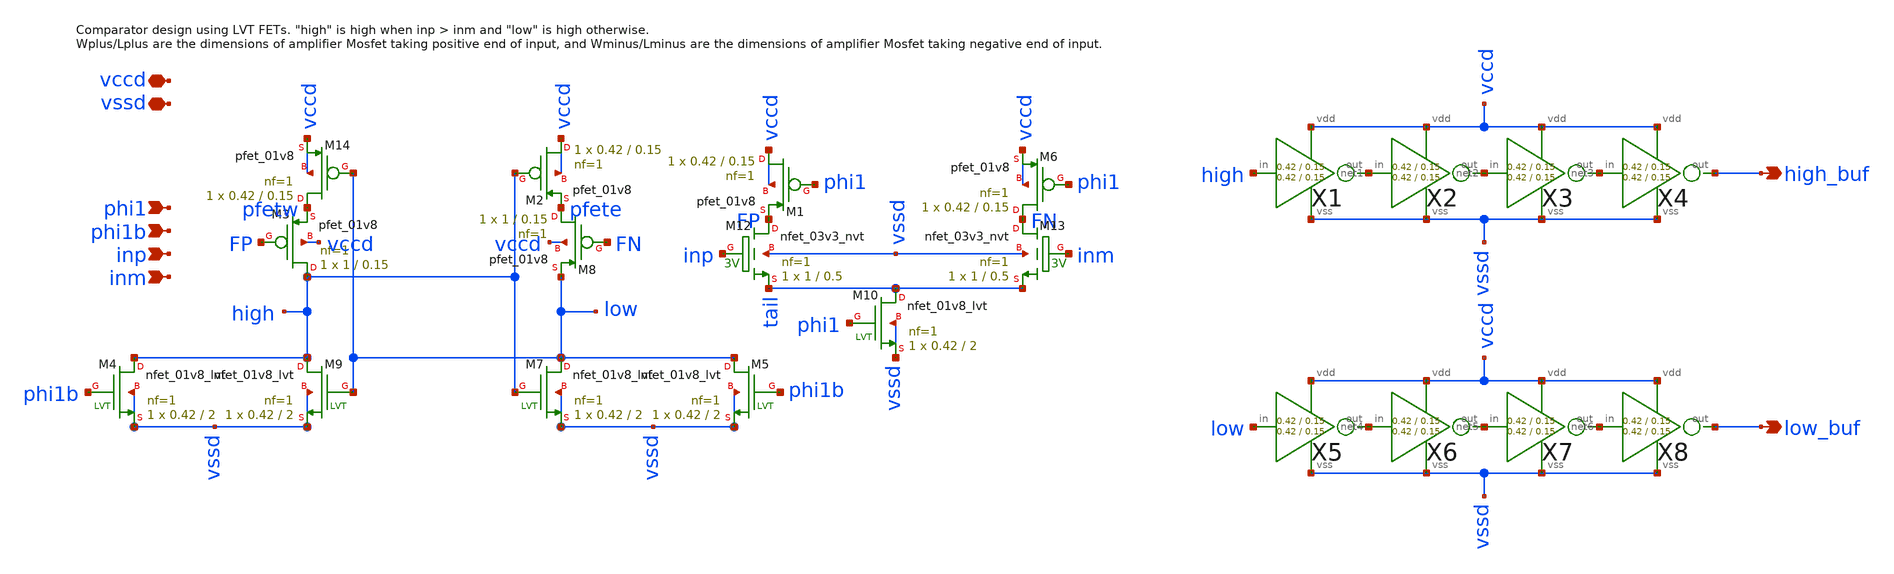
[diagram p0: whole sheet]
** sch_path: xschem/comparator_latest/comparator_single_tail.sch
**.subckt comparator_single_tail phi1 phi1b inp inm low_buf vccd vssd high_buf
*.ipin phi1
*.ipin phi1b
*.ipin inp
*.ipin inm
*.opin low_buf
*.iopin vccd
*.iopin vssd
*.opin high_buf
XM12 FP inp tail vssd sky130_fd_pr__nfet_03v3_nvt L=0.5 W=1 nf=1 ad='int((nf+1)/2) * W/nf * 0.29' as='int((nf+2)/2) * W/nf * 0.29'
+ pd='2*int((nf+1)/2) * (W/nf + 0.29)' ps='2*int((nf+2)/2) * (W/nf + 0.29)' nrd='0.29 / W' nrs='0.29 / W'
+ sa=0 sb=0 sd=0 mult=1 m=1
XM13 FN inm tail vssd sky130_fd_pr__nfet_03v3_nvt L=0.5 W=1 nf=1 ad='int((nf+1)/2) * W/nf * 0.29' as='int((nf+2)/2) * W/nf * 0.29'
+ pd='2*int((nf+1)/2) * (W/nf + 0.29)' ps='2*int((nf+2)/2) * (W/nf + 0.29)' nrd='0.29 / W' nrs='0.29 / W'
+ sa=0 sb=0 sd=0 mult=1 m=1
XM14 pfetw low vccd vccd sky130_fd_pr__pfet_01v8 L=0.15 W=0.42 nf=1 ad='int((nf+1)/2) * W/nf * 0.29'
+ as='int((nf+2)/2) * W/nf * 0.29' pd='2*int((nf+1)/2) * (W/nf + 0.29)' ps='2*int((nf+2)/2) * (W/nf + 0.29)'
+ nrd='0.29 / W' nrs='0.29 / W' sa=0 sb=0 sd=0 mult=1 m=1
XM3 high FP pfetw vccd sky130_fd_pr__pfet_01v8 L=0.15 W=1 nf=1 ad='int((nf+1)/2) * W/nf * 0.29' as='int((nf+2)/2) * W/nf * 0.29'
+ pd='2*int((nf+1)/2) * (W/nf + 0.29)' ps='2*int((nf+2)/2) * (W/nf + 0.29)' nrd='0.29 / W' nrs='0.29 / W'
+ sa=0 sb=0 sd=0 mult=1 m=1
XM8 pfete FN low vccd sky130_fd_pr__pfet_01v8 L=0.15 W=1 nf=1 ad='int((nf+1)/2) * W/nf * 0.29' as='int((nf+2)/2) * W/nf * 0.29'
+ pd='2*int((nf+1)/2) * (W/nf + 0.29)' ps='2*int((nf+2)/2) * (W/nf + 0.29)' nrd='0.29 / W' nrs='0.29 / W'
+ sa=0 sb=0 sd=0 mult=1 m=1
XM2 vccd high pfete vccd sky130_fd_pr__pfet_01v8 L=0.15 W=0.42 nf=1 ad='int((nf+1)/2) * W/nf * 0.29'
+ as='int((nf+2)/2) * W/nf * 0.29' pd='2*int((nf+1)/2) * (W/nf + 0.29)' ps='2*int((nf+2)/2) * (W/nf + 0.29)'
+ nrd='0.29 / W' nrs='0.29 / W' sa=0 sb=0 sd=0 mult=1 m=1
XM7 low high vssd vssd sky130_fd_pr__nfet_01v8_lvt L=2 W=0.42 nf=1 ad='int((nf+1)/2) * W/nf * 0.29' as='int((nf+2)/2) * W/nf * 0.29'
+ pd='2*int((nf+1)/2) * (W/nf + 0.29)' ps='2*int((nf+2)/2) * (W/nf + 0.29)' nrd='0.29 / W' nrs='0.29 / W'
+ sa=0 sb=0 sd=0 mult=1 m=1
XM9 high low vssd vssd sky130_fd_pr__nfet_01v8_lvt L=2 W=0.42 nf=1 ad='int((nf+1)/2) * W/nf * 0.29' as='int((nf+2)/2) * W/nf * 0.29'
+ pd='2*int((nf+1)/2) * (W/nf + 0.29)' ps='2*int((nf+2)/2) * (W/nf + 0.29)' nrd='0.29 / W' nrs='0.29 / W'
+ sa=0 sb=0 sd=0 mult=1 m=1
XM10 tail phi1 vssd vssd sky130_fd_pr__nfet_01v8_lvt L=2 W=0.42 nf=1 ad='int((nf+1)/2) * W/nf * 0.29'
+ as='int((nf+2)/2) * W/nf * 0.29' pd='2*int((nf+1)/2) * (W/nf + 0.29)' ps='2*int((nf+2)/2) * (W/nf + 0.29)'
+ nrd='0.29 / W' nrs='0.29 / W' sa=0 sb=0 sd=0 mult=1 m=1
XM1 vccd phi1 FP vccd sky130_fd_pr__pfet_01v8 L=0.15 W=0.42 nf=1 ad='int((nf+1)/2) * W/nf * 0.29' as='int((nf+2)/2) * W/nf * 0.29'
+ pd='2*int((nf+1)/2) * (W/nf + 0.29)' ps='2*int((nf+2)/2) * (W/nf + 0.29)' nrd='0.29 / W' nrs='0.29 / W'
+ sa=0 sb=0 sd=0 mult=1 m=1
XM6 FN phi1 vccd vccd sky130_fd_pr__pfet_01v8 L=0.15 W=0.42 nf=1 ad='int((nf+1)/2) * W/nf * 0.29' as='int((nf+2)/2) * W/nf * 0.29'
+ pd='2*int((nf+1)/2) * (W/nf + 0.29)' ps='2*int((nf+2)/2) * (W/nf + 0.29)' nrd='0.29 / W' nrs='0.29 / W'
+ sa=0 sb=0 sd=0 mult=1 m=1
X1 high net1 vccd vssd inv Wpmos=0.42 Lpmos=0.15 Wnmos=0.42 Lnmos=0.15
X2 net1 net2 vccd vssd inv Wpmos=0.42 Lpmos=0.15 Wnmos=0.42 Lnmos=0.15
X3 net2 net3 vccd vssd inv Wpmos=0.42 Lpmos=0.15 Wnmos=0.42 Lnmos=0.15
X4 net3 high_buf vccd vssd inv Wpmos=0.42 Lpmos=0.15 Wnmos=0.42 Lnmos=0.15
X5 low net4 vccd vssd inv Wpmos=0.42 Lpmos=0.15 Wnmos=0.42 Lnmos=0.15
X6 net4 net5 vccd vssd inv Wpmos=0.42 Lpmos=0.15 Wnmos=0.42 Lnmos=0.15
X7 net5 net6 vccd vssd inv Wpmos=0.42 Lpmos=0.15 Wnmos=0.42 Lnmos=0.15
X8 net6 low_buf vccd vssd inv Wpmos=0.42 Lpmos=0.15 Wnmos=0.42 Lnmos=0.15
XM4 high phi1b vssd vssd sky130_fd_pr__nfet_01v8_lvt L=2 W=0.42 nf=1 ad='int((nf+1)/2) * W/nf * 0.29'
+ as='int((nf+2)/2) * W/nf * 0.29' pd='2*int((nf+1)/2) * (W/nf + 0.29)' ps='2*int((nf+2)/2) * (W/nf + 0.29)'
+ nrd='0.29 / W' nrs='0.29 / W' sa=0 sb=0 sd=0 mult=1 m=1
XM5 low phi1b vssd vssd sky130_fd_pr__nfet_01v8_lvt L=2 W=0.42 nf=1 ad='int((nf+1)/2) * W/nf * 0.29'
+ as='int((nf+2)/2) * W/nf * 0.29' pd='2*int((nf+1)/2) * (W/nf + 0.29)' ps='2*int((nf+2)/2) * (W/nf + 0.29)'
+ nrd='0.29 / W' nrs='0.29 / W' sa=0 sb=0 sd=0 mult=1 m=1
**.ends

* expanding   symbol:  xschem/inv/inv.sym # of pins=4
** sym_path: xschem/inv/inv.sym
** sch_path: xschem/inv/inv.sch
.subckt inv in out vdd vss  Wpmos=Wpmos Lpmos=Lpmos Wnmos=Wnmos Lnmos=Lnmos
*.ipin in
*.iopin out
*.iopin vdd
*.iopin vss
XM1 vss in out vss sky130_fd_pr__nfet_01v8 L=Lnmos W=Wnmos nf=1 ad='int((nf+1)/2) * W/nf * 0.29' as='int((nf+2)/2) * W/nf * 0.29'
+ pd='2*int((nf+1)/2) * (W/nf + 0.29)' ps='2*int((nf+2)/2) * (W/nf + 0.29)' nrd='0.29 / W' nrs='0.29 / W'
+ sa=0 sb=0 sd=0 mult=1 m=1
XM2 vdd in out vdd sky130_fd_pr__pfet_01v8 L=Lpmos W=Wpmos nf=1 ad='int((nf+1)/2) * W/nf * 0.29' as='int((nf+2)/2) * W/nf * 0.29'
+ pd='2*int((nf+1)/2) * (W/nf + 0.29)' ps='2*int((nf+2)/2) * (W/nf + 0.29)' nrd='0.29 / W' nrs='0.29 / W'
+ sa=0 sb=0 sd=0 mult=1 m=1
.ends

.end
